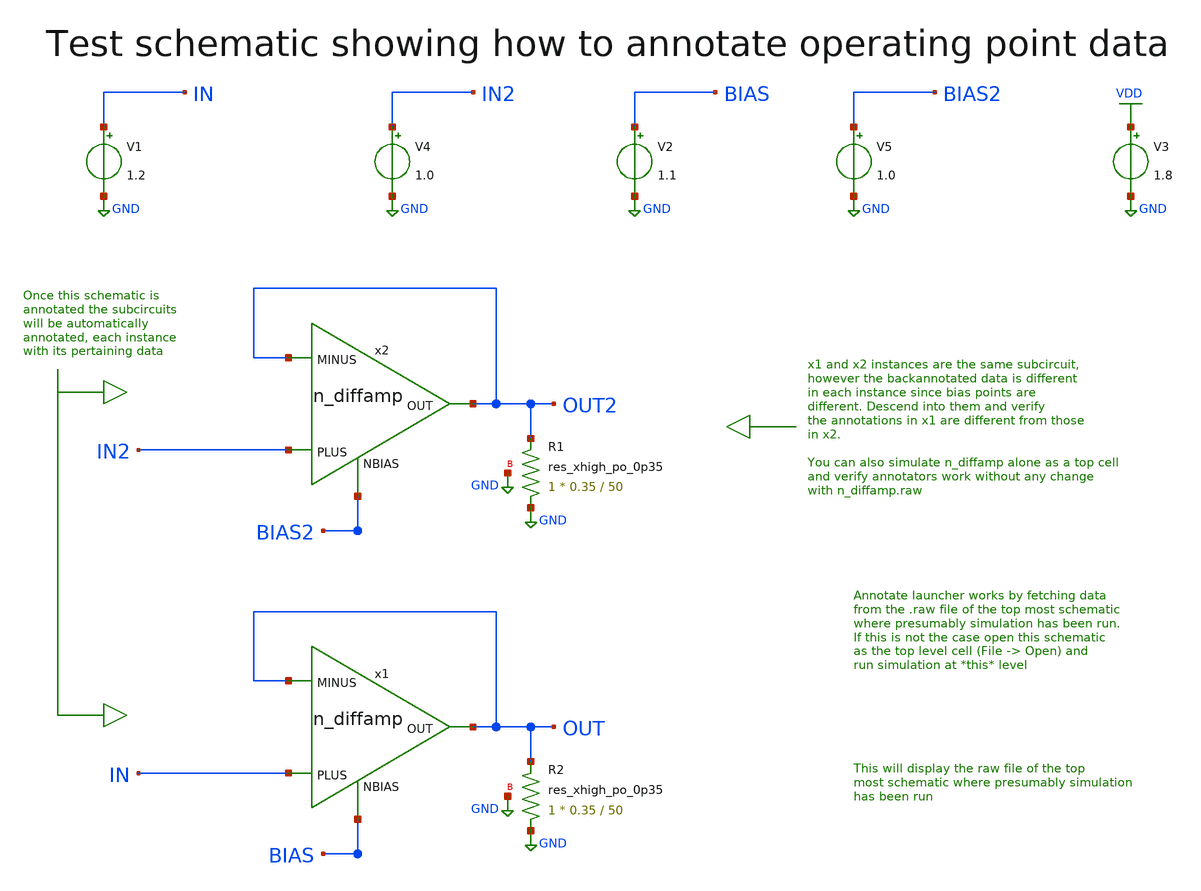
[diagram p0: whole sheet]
** sch_path: xyce/sky130A-xyce/libs.tech/xschem/sky130_tests/test_analog.sch
* Copyright 2020 Stefan Frederik Schippers
* Licensed under the Apache License, Version 2.0 (the "License");
* you may not use this file except in compliance with the License.
* You may obtain a copy of the License at
* https://www.apache.org/licenses/LICENSE-2.0
* Unless required by applicable law or agreed to in writing, software
* distributed under the License is distributed on an "AS IS" BASIS,
* WITHOUT WARRANTIES OR CONDITIONS OF ANY KIND, either express or implied.
* See the License for the specific language governing permissions and
* limitations under the License.
**.subckt test_analog
x1 OUT OUT IN BIAS n_diffamp
x2 OUT2 OUT2 IN2 BIAS2 n_diffamp
V1 IN GND 1.2
V2 BIAS GND 1.1
V3 VDD GND 1.8
V4 IN2 GND 1.0
V5 BIAS2 GND 1.0
XR1 GND OUT2 GND sky130_fd_pr__res_xhigh_po_0p35 W=0.35 L=50 mult=1 m=1
XR2 GND OUT GND sky130_fd_pr__res_xhigh_po_0p35 W=0.35 L=50 mult=1 m=1
**** begin user architecture code

.include $::SKYWATER_MODELS/cells/nfet_01v8/sky130_fd_pr__nfet_01v8__tt.corner.spice
.include $::SKYWATER_MODELS/cells/nfet_01v8_lvt/sky130_fd_pr__nfet_01v8_lvt__tt.corner.spice
.include $::SKYWATER_MODELS/cells/pfet_01v8/sky130_fd_pr__pfet_01v8__tt.corner.spice
.include $::SKYWATER_MODELS/cells/nfet_03v3_nvt/sky130_fd_pr__nfet_03v3_nvt__tt.corner.spice
.include $::SKYWATER_MODELS/cells/nfet_05v0_nvt/sky130_fd_pr__nfet_05v0_nvt__tt.corner.spice
.include $::SKYWATER_MODELS/cells/esd_nfet_01v8/sky130_fd_pr__esd_nfet_01v8__tt.corner.spice
.include $::SKYWATER_MODELS/cells/pfet_01v8_lvt/sky130_fd_pr__pfet_01v8_lvt__tt.corner.spice
.include $::SKYWATER_MODELS/cells/pfet_01v8_hvt/sky130_fd_pr__pfet_01v8_hvt__tt.corner.spice
.include $::SKYWATER_MODELS/cells/esd_pfet_g5v0d10v5/sky130_fd_pr__esd_pfet_g5v0d10v5__tt.corner.spice
.include $::SKYWATER_MODELS/cells/pfet_g5v0d10v5/sky130_fd_pr__pfet_g5v0d10v5__tt.corner.spice
.include $::SKYWATER_MODELS/cells/pfet_g5v0d16v0/sky130_fd_pr__pfet_g5v0d16v0__tt.corner.spice
.include $::SKYWATER_MODELS/cells/nfet_g5v0d10v5/sky130_fd_pr__nfet_g5v0d10v5__tt.corner.spice
.include $::SKYWATER_MODELS/cells/nfet_g5v0d16v0/sky130_fd_pr__nfet_g5v0d16v0__tt_discrete.corner.spice
.include $::SKYWATER_MODELS/cells/esd_nfet_g5v0d10v5/sky130_fd_pr__esd_nfet_g5v0d10v5__tt.corner.spice
.include $::SKYWATER_MODELS/models/corners/tt/nonfet.spice
* Mismatch parameters
.include $::SKYWATER_MODELS/cells/nfet_01v8/sky130_fd_pr__nfet_01v8__mismatch.corner.spice
.include $::SKYWATER_MODELS/cells/pfet_01v8/sky130_fd_pr__pfet_01v8__mismatch.corner.spice
.include $::SKYWATER_MODELS/cells/nfet_01v8_lvt/sky130_fd_pr__nfet_01v8_lvt__mismatch.corner.spice
.include $::SKYWATER_MODELS/cells/pfet_01v8_lvt/sky130_fd_pr__pfet_01v8_lvt__mismatch.corner.spice
.include $::SKYWATER_MODELS/cells/pfet_01v8_hvt/sky130_fd_pr__pfet_01v8_hvt__mismatch.corner.spice
.include $::SKYWATER_MODELS/cells/nfet_g5v0d10v5/sky130_fd_pr__nfet_g5v0d10v5__mismatch.corner.spice
.include $::SKYWATER_MODELS/cells/pfet_g5v0d10v5/sky130_fd_pr__pfet_g5v0d10v5__mismatch.corner.spice
.include $::SKYWATER_MODELS/cells/nfet_05v0_nvt/sky130_fd_pr__nfet_05v0_nvt__mismatch.corner.spice
.include $::SKYWATER_MODELS/cells/nfet_03v3_nvt/sky130_fd_pr__nfet_03v3_nvt__mismatch.corner.spice
* Resistor$::SKYWATER_MODELS/Capacitor
.include $::SKYWATER_MODELS/models/r+c/res_typical__cap_typical.spice
.include $::SKYWATER_MODELS/models/r+c/res_typical__cap_typical__lin.spice
* Special cells
.include $::SKYWATER_MODELS/models/corners/tt/specialized_cells.spice
* All models
.include $::SKYWATER_MODELS/models/all.spice
* Corner
.include $::SKYWATER_MODELS/models/corners/tt/rf.spice

**** end user architecture code
**.ends

* expanding   symbol:  sky130_tests/n_diffamp.sym # of pins=4
** sym_path: xyce/sky130A-xyce/libs.tech/xschem/sky130_tests/n_diffamp.sym
** sch_path: xyce/sky130A-xyce/libs.tech/xschem/sky130_tests/n_diffamp.sch
.subckt n_diffamp OUT MINUS PLUS NBIAS
*.ipin PLUS
*.ipin MINUS
*.opin OUT
*.ipin NBIAS
XM1 net1 PLUS S GND sky130_fd_pr__nfet_01v8_lvt L=0.3 W=2 nf=1 ad='int((nf+1)/2) * W/nf * 0.29' as='int((nf+2)/2) * W/nf * 0.29'
+ pd='2*int((nf+1)/2) * (W/nf + 0.29)' ps='2*int((nf+2)/2) * (W/nf + 0.29)' nrd='0.29 / W' nrs='0.29 / W'
+ sa=0 sb=0 sd=0 mult=1 m=1
XM2 OUT MINUS S GND sky130_fd_pr__nfet_01v8_lvt L=0.3 W=2 nf=1 ad='int((nf+1)/2) * W/nf * 0.29' as='int((nf+2)/2) * W/nf * 0.29'
+ pd='2*int((nf+1)/2) * (W/nf + 0.29)' ps='2*int((nf+2)/2) * (W/nf + 0.29)' nrd='0.29 / W' nrs='0.29 / W'
+ sa=0 sb=0 sd=0 mult=1 m=1
XM3 OUT net1 VDD VDD sky130_fd_pr__pfet_01v8_lvt L=0.8 W=4 nf=1 ad='int((nf+1)/2) * W/nf * 0.29' as='int((nf+2)/2) * W/nf * 0.29'
+ pd='2*int((nf+1)/2) * (W/nf + 0.29)' ps='2*int((nf+2)/2) * (W/nf + 0.29)' nrd='0.29 / W' nrs='0.29 / W'
+ sa=0 sb=0 sd=0 mult=1 m=1
XM4 net1 net1 VDD VDD sky130_fd_pr__pfet_01v8_lvt L=0.8 W=4 nf=1 ad='int((nf+1)/2) * W/nf * 0.29' as='int((nf+2)/2) * W/nf * 0.29'
+ pd='2*int((nf+1)/2) * (W/nf + 0.29)' ps='2*int((nf+2)/2) * (W/nf + 0.29)' nrd='0.29 / W' nrs='0.29 / W'
+ sa=0 sb=0 sd=0 mult=1 m=1
XM5 net2 NBIAS GND GND sky130_fd_pr__nfet_01v8 L=1.2 W=0.7 nf=1 ad='int((nf+1)/2) * W/nf * 0.29' as='int((nf+2)/2) * W/nf * 0.29'
+ pd='2*int((nf+1)/2) * (W/nf + 0.29)' ps='2*int((nf+2)/2) * (W/nf + 0.29)' nrd='0.29 / W' nrs='0.29 / W'
+ sa=0 sb=0 sd=0 mult=1 m=1
XR1 GND S GND sky130_fd_pr__res_xhigh_po_0p35 W=0.35 L=50 mult=1 m=1
V5 S net2 0
.ends

.GLOBAL GND
.GLOBAL VDD
**** begin user architecture code



.options savecurrents
.control
save all
save @m.x1.xm5.msky130_fd_pr__nfet_01v8[gm]
save @m.x2.xm5.msky130_fd_pr__nfet_01v8[gm]
op
write test_analog.raw
.endc


**** end user architecture code
.end
